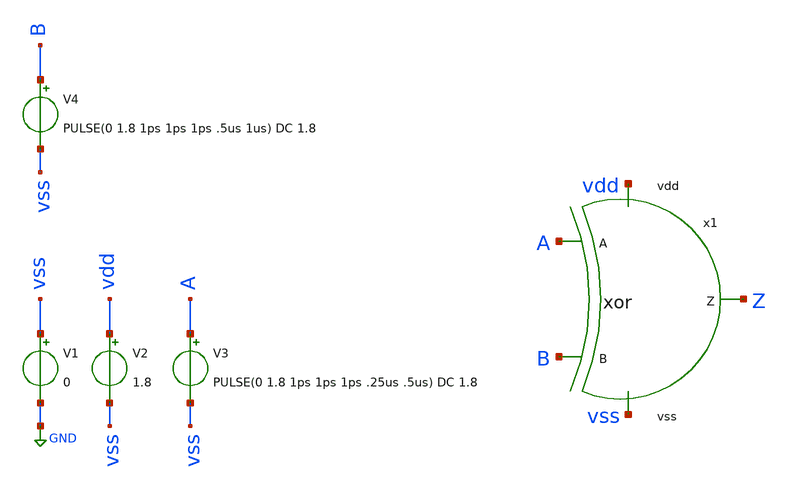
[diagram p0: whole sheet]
** sch_path: track_vlsi/somoza/sch/tb_xor.sch
**.subckt tb_xor
V1 vss GND 0
V2 vdd vss 1.8
V3 A vss PULSE(0 1.8 1ps 1ps 1ps .25us .5us) DC 1.8
V4 B vss PULSE(0 1.8 1ps 1ps 1ps .5us 1us) DC 1.8
x1 Z A B vdd vss xor
**** begin user architecture code



* Parametros del circuito

.options TEMP = 27.0

* Include
.lib /home/eamta/skywater/skywater-pdk/libraries/sky130_fd_pr_ngspice/latest/models/corners/sky130.lib TT

* Signals to SAVE
*.save all
*+ @M.x1.XM1.msky130_fd_pr__nfet_01v8[id] @M.x1.XM1.msky130_fd_pr__nfet_01v8[gm]
*+ @M.x1.XM2.msky130_fd_pr__pfet_01v8[id] @M.x1.XM2.msky130_fd_pr__pfet_01v8[gm]

* Simulation
.control
  tran .001u 1us
  setplot tran1
  plot v(A)
  plot v(B)
  plot v(Z)
  write tb_xor_tran.raw

.endc

.end


**** end user architecture code
**.ends
.GLOBAL GND
.end
